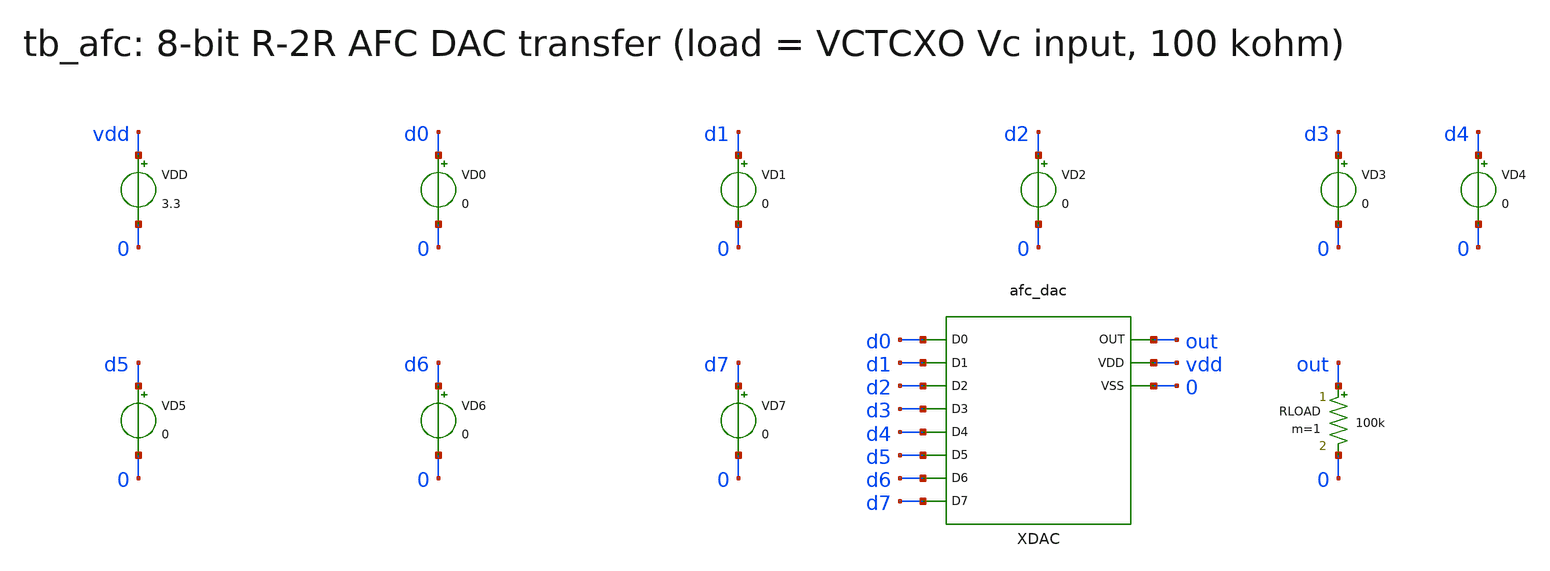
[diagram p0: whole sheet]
** sch_path: v1_claude/xschem/tb_afc.sch
**.subckt tb_afc
VDD vdd 0 3.3
VD0 d0 0 0
VD1 d1 0 0
VD2 d2 0 0
VD3 d3 0 0
VD4 d4 0 0
VD5 d5 0 0
VD6 d6 0 0
VD7 d7 0 0
XDAC d0 d1 d2 d3 d4 d5 d6 d7 out vdd 0 afc_dac
RLOAD out 0 100k m=1
**** begin user architecture code
 .include $::180MCU_MODELS/design.ngspice
.lib $::180MCU_MODELS/sm141064.ngspice typical
.lib $::180MCU_MODELS/sm141064.ngspice res_typical
.lib $::180MCU_MODELS/sm141064.ngspice mimcap_typical

.control
set num_threads=1
alter VD0 dc = 0
alter VD1 dc = 0
alter VD2 dc = 0
alter VD3 dc = 0
alter VD4 dc = 0
alter VD5 dc = 0
alter VD6 dc = 0
alter VD7 dc = 0
op
echo DAC 0 $&v(out)
alter VD0 dc = 3.3
alter VD1 dc = 0
alter VD2 dc = 0
alter VD3 dc = 0
alter VD4 dc = 0
alter VD5 dc = 0
alter VD6 dc = 0
alter VD7 dc = 0
op
echo DAC 1 $&v(out)
alter VD0 dc = 0
alter VD1 dc = 3.3
alter VD2 dc = 0
alter VD3 dc = 0
alter VD4 dc = 0
alter VD5 dc = 0
alter VD6 dc = 0
alter VD7 dc = 0
op
echo DAC 2 $&v(out)
alter VD0 dc = 3.3
alter VD1 dc = 3.3
alter VD2 dc = 0
alter VD3 dc = 0
alter VD4 dc = 0
alter VD5 dc = 0
alter VD6 dc = 0
alter VD7 dc = 0
op
echo DAC 3 $&v(out)
alter VD0 dc = 0
alter VD1 dc = 0
alter VD2 dc = 3.3
alter VD3 dc = 0
alter VD4 dc = 0
alter VD5 dc = 0
alter VD6 dc = 0
alter VD7 dc = 0
op
echo DAC 4 $&v(out)
alter VD0 dc = 3.3
alter VD1 dc = 0
alter VD2 dc = 3.3
alter VD3 dc = 0
alter VD4 dc = 0
alter VD5 dc = 0
alter VD6 dc = 0
alter VD7 dc = 0
op
echo DAC 5 $&v(out)
alter VD0 dc = 0
alter VD1 dc = 3.3
alter VD2 dc = 3.3
alter VD3 dc = 0
alter VD4 dc = 0
alter VD5 dc = 0
alter VD6 dc = 0
alter VD7 dc = 0
op
echo DAC 6 $&v(out)
alter VD0 dc = 3.3
alter VD1 dc = 3.3
alter VD2 dc = 3.3
alter VD3 dc = 0
alter VD4 dc = 0
alter VD5 dc = 0
alter VD6 dc = 0
alter VD7 dc = 0
op
echo DAC 7 $&v(out)
alter VD0 dc = 0
alter VD1 dc = 0
alter VD2 dc = 0
alter VD3 dc = 3.3
alter VD4 dc = 0
alter VD5 dc = 0
alter VD6 dc = 0
alter VD7 dc = 0
op
echo DAC 8 $&v(out)
alter VD0 dc = 3.3
alter VD1 dc = 0
alter VD2 dc = 0
alter VD3 dc = 3.3
alter VD4 dc = 0
alter VD5 dc = 0
alter VD6 dc = 0
alter VD7 dc = 0
op
echo DAC 9 $&v(out)
alter VD0 dc = 0
alter VD1 dc = 3.3
alter VD2 dc = 0
alter VD3 dc = 3.3
alter VD4 dc = 0
alter VD5 dc = 0
alter VD6 dc = 0
alter VD7 dc = 0
op
echo DAC 10 $&v(out)
alter VD0 dc = 3.3
alter VD1 dc = 3.3
alter VD2 dc = 0
alter VD3 dc = 3.3
alter VD4 dc = 0
alter VD5 dc = 0
alter VD6 dc = 0
alter VD7 dc = 0
op
echo DAC 11 $&v(out)
alter VD0 dc = 0
alter VD1 dc = 0
alter VD2 dc = 3.3
alter VD3 dc = 3.3
alter VD4 dc = 0
alter VD5 dc = 0
alter VD6 dc = 0
alter VD7 dc = 0
op
echo DAC 12 $&v(out)
alter VD0 dc = 3.3
alter VD1 dc = 0
alter VD2 dc = 3.3
alter VD3 dc = 3.3
alter VD4 dc = 0
alter VD5 dc = 0
alter VD6 dc = 0
alter VD7 dc = 0
op
echo DAC 13 $&v(out)
alter VD0 dc = 0
alter VD1 dc = 3.3
alter VD2 dc = 3.3
alter VD3 dc = 3.3
alter VD4 dc = 0
alter VD5 dc = 0
alter VD6 dc = 0
alter VD7 dc = 0
op
echo DAC 14 $&v(out)
alter VD0 dc = 3.3
alter VD1 dc = 3.3
alter VD2 dc = 3.3
alter VD3 dc = 3.3
alter VD4 dc = 0
alter VD5 dc = 0
alter VD6 dc = 0
alter VD7 dc = 0
op
echo DAC 15 $&v(out)
alter VD0 dc = 0
alter VD1 dc = 0
alter VD2 dc = 0
alter VD3 dc = 0
alter VD4 dc = 3.3
alter VD5 dc = 0
alter VD6 dc = 0
alter VD7 dc = 0
op
echo DAC 16 $&v(out)
alter VD0 dc = 3.3
alter VD1 dc = 0
alter VD2 dc = 0
alter VD3 dc = 0
alter VD4 dc = 3.3
alter VD5 dc = 0
alter VD6 dc = 0
alter VD7 dc = 0
op
echo DAC 17 $&v(out)
alter VD0 dc = 0
alter VD1 dc = 3.3
alter VD2 dc = 0
alter VD3 dc = 0
alter VD4 dc = 3.3
alter VD5 dc = 0
alter VD6 dc = 0
alter VD7 dc = 0
op
echo DAC 18 $&v(out)
alter VD0 dc = 3.3
alter VD1 dc = 3.3
alter VD2 dc = 0
alter VD3 dc = 0
alter VD4 dc = 3.3
alter VD5 dc = 0
alter VD6 dc = 0
alter VD7 dc = 0
op
echo DAC 19 $&v(out)
alter VD0 dc = 0
alter VD1 dc = 0
alter VD2 dc = 3.3
alter VD3 dc = 0
alter VD4 dc = 3.3
alter VD5 dc = 0
alter VD6 dc = 0
alter VD7 dc = 0
op
echo DAC 20 $&v(out)
alter VD0 dc = 3.3
alter VD1 dc = 0
alter VD2 dc = 3.3
alter VD3 dc = 0
alter VD4 dc = 3.3
alter VD5 dc = 0
alter VD6 dc = 0
alter VD7 dc = 0
op
echo DAC 21 $&v(out)
alter VD0 dc = 0
alter VD1 dc = 3.3
alter VD2 dc = 3.3
alter VD3 dc = 0
alter VD4 dc = 3.3
alter VD5 dc = 0
alter VD6 dc = 0
alter VD7 dc = 0
op
echo DAC 22 $&v(out)
alter VD0 dc = 3.3
alter VD1 dc = 3.3
alter VD2 dc = 3.3
alter VD3 dc = 0
alter VD4 dc = 3.3
alter VD5 dc = 0
alter VD6 dc = 0
alter VD7 dc = 0
op
echo DAC 23 $&v(out)
alter VD0 dc = 0
alter VD1 dc = 0
alter VD2 dc = 0
alter VD3 dc = 3.3
alter VD4 dc = 3.3
alter VD5 dc = 0
alter VD6 dc = 0
alter VD7 dc = 0
op
echo DAC 24 $&v(out)
alter VD0 dc = 3.3
alter VD1 dc = 0
alter VD2 dc = 0
alter VD3 dc = 3.3
alter VD4 dc = 3.3
alter VD5 dc = 0
alter VD6 dc = 0
alter VD7 dc = 0
op
echo DAC 25 $&v(out)
alter VD0 dc = 0
alter VD1 dc = 3.3
alter VD2 dc = 0
alter VD3 dc = 3.3
alter VD4 dc = 3.3
alter VD5 dc = 0
alter VD6 dc = 0
alter VD7 dc = 0
op
echo DAC 26 $&v(out)
alter VD0 dc = 3.3
alter VD1 dc = 3.3
alter VD2 dc = 0
alter VD3 dc = 3.3
alter VD4 dc = 3.3
alter VD5 dc = 0
alter VD6 dc = 0
alter VD7 dc = 0
op
echo DAC 27 $&v(out)
alter VD0 dc = 0
alter VD1 dc = 0
alter VD2 dc = 3.3
alter VD3 dc = 3.3
alter VD4 dc = 3.3
alter VD5 dc = 0
alter VD6 dc = 0
alter VD7 dc = 0
op
echo DAC 28 $&v(out)
alter VD0 dc = 3.3
alter VD1 dc = 0
alter VD2 dc = 3.3
alter VD3 dc = 3.3
alter VD4 dc = 3.3
alter VD5 dc = 0
alter VD6 dc = 0
alter VD7 dc = 0
op
echo DAC 29 $&v(out)
alter VD0 dc = 0
alter VD1 dc = 3.3
alter VD2 dc = 3.3
alter VD3 dc = 3.3
alter VD4 dc = 3.3
alter VD5 dc = 0
alter VD6 dc = 0
alter VD7 dc = 0
op
echo DAC 30 $&v(out)
alter VD0 dc = 3.3
alter VD1 dc = 3.3
alter VD2 dc = 3.3
alter VD3 dc = 3.3
alter VD4 dc = 3.3
alter VD5 dc = 0
alter VD6 dc = 0
alter VD7 dc = 0
op
echo DAC 31 $&v(out)
alter VD0 dc = 0
alter VD1 dc = 0
alter VD2 dc = 0
alter VD3 dc = 0
alter VD4 dc = 0
alter VD5 dc = 3.3
alter VD6 dc = 0
alter VD7 dc = 0
op
echo DAC 32 $&v(out)
alter VD0 dc = 3.3
alter VD1 dc = 0
alter VD2 dc = 0
alter VD3 dc = 0
alter VD4 dc = 0
alter VD5 dc = 3.3
alter VD6 dc = 0
alter VD7 dc = 0
op
echo DAC 33 $&v(out)
alter VD0 dc = 0
alter VD1 dc = 3.3
alter VD2 dc = 0
alter VD3 dc = 0
alter VD4 dc = 0
alter VD5 dc = 3.3
alter VD6 dc = 0
alter VD7 dc = 0
op
echo DAC 34 $&v(out)
alter VD0 dc = 3.3
alter VD1 dc = 3.3
alter VD2 dc = 0
alter VD3 dc = 0
alter VD4 dc = 0
alter VD5 dc = 3.3
alter VD6 dc = 0
alter VD7 dc = 0
op
echo DAC 35 $&v(out)
alter VD0 dc = 0
alter VD1 dc = 0
alter VD2 dc = 3.3
alter VD3 dc = 0
alter VD4 dc = 0
alter VD5 dc = 3.3
alter VD6 dc = 0
alter VD7 dc = 0
op
echo DAC 36 $&v(out)
alter VD0 dc = 3.3
alter VD1 dc = 0
alter VD2 dc = 3.3
alter VD3 dc = 0
alter VD4 dc = 0
alter VD5 dc = 3.3
alter VD6 dc = 0
alter VD7 dc = 0
op
echo DAC 37 $&v(out)
alter VD0 dc = 0
alter VD1 dc = 3.3
alter VD2 dc = 3.3
alter VD3 dc = 0
alter VD4 dc = 0
alter VD5 dc = 3.3
alter VD6 dc = 0
alter VD7 dc = 0
op
echo DAC 38 $&v(out)
alter VD0 dc = 3.3
alter VD1 dc = 3.3
alter VD2 dc = 3.3
alter VD3 dc = 0
alter VD4 dc = 0
alter VD5 dc = 3.3
alter VD6 dc = 0
alter VD7 dc = 0
op
echo DAC 39 $&v(out)
alter VD0 dc = 0
alter VD1 dc = 0
alter VD2 dc = 0
alter VD3 dc = 3.3
alter VD4 dc = 0
alter VD5 dc = 3.3
alter VD6 dc = 0
alter VD7 dc = 0
op
echo DAC 40 $&v(out)
alter VD0 dc = 3.3
alter VD1 dc = 0
alter VD2 dc = 0
alter VD3 dc = 3.3
alter VD4 dc = 0
alter VD5 dc = 3.3
alter VD6 dc = 0
alter VD7 dc = 0
op
echo DAC 41 $&v(out)
alter VD0 dc = 0
alter VD1 dc = 3.3
alter VD2 dc = 0
alter VD3 dc = 3.3
alter VD4 dc = 0
alter VD5 dc = 3.3
alter VD6 dc = 0
alter VD7 dc = 0
op
echo DAC 42 $&v(out)
alter VD0 dc = 3.3
alter VD1 dc = 3.3
alter VD2 dc = 0
alter VD3 dc = 3.3
alter VD4 dc = 0
alter VD5 dc = 3.3
alter VD6 dc = 0
alter VD7 dc = 0
op
echo DAC 43 $&v(out)
alter VD0 dc = 0
alter VD1 dc = 0
alter VD2 dc = 3.3
alter VD3 dc = 3.3
alter VD4 dc = 0
alter VD5 dc = 3.3
alter VD6 dc = 0
alter VD7 dc = 0
op
echo DAC 44 $&v(out)
alter VD0 dc = 3.3
alter VD1 dc = 0
alter VD2 dc = 3.3
alter VD3 dc = 3.3
alter VD4 dc = 0
alter VD5 dc = 3.3
alter VD6 dc = 0
alter VD7 dc = 0
op
echo DAC 45 $&v(out)
alter VD0 dc = 0
alter VD1 dc = 3.3
alter VD2 dc = 3.3
alter VD3 dc = 3.3
alter VD4 dc = 0
alter VD5 dc = 3.3
alter VD6 dc = 0
alter VD7 dc = 0
op
echo DAC 46 $&v(out)
alter VD0 dc = 3.3
alter VD1 dc = 3.3
alter VD2 dc = 3.3
alter VD3 dc = 3.3
alter VD4 dc = 0
alter VD5 dc = 3.3
alter VD6 dc = 0
alter VD7 dc = 0
op
echo DAC 47 $&v(out)
alter VD0 dc = 0
alter VD1 dc = 0
alter VD2 dc = 0
alter VD3 dc = 0
alter VD4 dc = 3.3
alter VD5 dc = 3.3
alter VD6 dc = 0
alter VD7 dc = 0
op
echo DAC 48 $&v(out)
alter VD0 dc = 3.3
alter VD1 dc = 0
alter VD2 dc = 0
alter VD3 dc = 0
alter VD4 dc = 3.3
alter VD5 dc = 3.3
alter VD6 dc = 0
alter VD7 dc = 0
op
echo DAC 49 $&v(out)
alter VD0 dc = 0
alter VD1 dc = 3.3
alter VD2 dc = 0
alter VD3 dc = 0
alter VD4 dc = 3.3
alter VD5 dc = 3.3
alter VD6 dc = 0
alter VD7 dc = 0
op
echo DAC 50 $&v(out)
alter VD0 dc = 3.3
alter VD1 dc = 3.3
alter VD2 dc = 0
alter VD3 dc = 0
alter VD4 dc = 3.3
alter VD5 dc = 3.3
alter VD6 dc = 0
alter VD7 dc = 0
op
echo DAC 51 $&v(out)
alter VD0 dc = 0
alter VD1 dc = 0
alter VD2 dc = 3.3
alter VD3 dc = 0
alter VD4 dc = 3.3
alter VD5 dc = 3.3
alter VD6 dc = 0
alter VD7 dc = 0
op
echo DAC 52 $&v(out)
alter VD0 dc = 3.3
alter VD1 dc = 0
alter VD2 dc = 3.3
alter VD3 dc = 0
alter VD4 dc = 3.3
alter VD5 dc = 3.3
alter VD6 dc = 0
alter VD7 dc = 0
op
echo DAC 53 $&v(out)
alter VD0 dc = 0
alter VD1 dc = 3.3
alter VD2 dc = 3.3
alter VD3 dc = 0
alter VD4 dc = 3.3
alter VD5 dc = 3.3
alter VD6 dc = 0
alter VD7 dc = 0
op
echo DAC 54 $&v(out)
alter VD0 dc = 3.3
alter VD1 dc = 3.3
alter VD2 dc = 3.3
alter VD3 dc = 0
alter VD4 dc = 3.3
alter VD5 dc = 3.3
alter VD6 dc = 0
alter VD7 dc = 0
op
echo DAC 55 $&v(out)
alter VD0 dc = 0
alter VD1 dc = 0
alter VD2 dc = 0
alter VD3 dc = 3.3
alter VD4 dc = 3.3
alter VD5 dc = 3.3
alter VD6 dc = 0
alter VD7 dc = 0
op
echo DAC 56 $&v(out)
alter VD0 dc = 3.3
alter VD1 dc = 0
alter VD2 dc = 0
alter VD3 dc = 3.3
alter VD4 dc = 3.3
alter VD5 dc = 3.3
alter VD6 dc = 0
alter VD7 dc = 0
op
echo DAC 57 $&v(out)
alter VD0 dc = 0
alter VD1 dc = 3.3
alter VD2 dc = 0
alter VD3 dc = 3.3
alter VD4 dc = 3.3
alter VD5 dc = 3.3
alter VD6 dc = 0
alter VD7 dc = 0
op
echo DAC 58 $&v(out)
alter VD0 dc = 3.3
alter VD1 dc = 3.3
alter VD2 dc = 0
alter VD3 dc = 3.3
alter VD4 dc = 3.3
alter VD5 dc = 3.3
alter VD6 dc = 0
alter VD7 dc = 0
op
echo DAC 59 $&v(out)
alter VD0 dc = 0
alter VD1 dc = 0
alter VD2 dc = 3.3
alter VD3 dc = 3.3
alter VD4 dc = 3.3
alter VD5 dc = 3.3
alter VD6 dc = 0
alter VD7 dc = 0
op
echo DAC 60 $&v(out)
alter VD0 dc = 3.3
alter VD1 dc = 0
alter VD2 dc = 3.3
alter VD3 dc = 3.3
alter VD4 dc = 3.3
alter VD5 dc = 3.3
alter VD6 dc = 0
alter VD7 dc = 0
op
echo DAC 61 $&v(out)
alter VD0 dc = 0
alter VD1 dc = 3.3
alter VD2 dc = 3.3
alter VD3 dc = 3.3
alter VD4 dc = 3.3
alter VD5 dc = 3.3
alter VD6 dc = 0
alter VD7 dc = 0
op
echo DAC 62 $&v(out)
alter VD0 dc = 3.3
alter VD1 dc = 3.3
alter VD2 dc = 3.3
alter VD3 dc = 3.3
alter VD4 dc = 3.3
alter VD5 dc = 3.3
alter VD6 dc = 0
alter VD7 dc = 0
op
echo DAC 63 $&v(out)
alter VD0 dc = 0
alter VD1 dc = 0
alter VD2 dc = 0
alter VD3 dc = 0
alter VD4 dc = 0
alter VD5 dc = 0
alter VD6 dc = 3.3
alter VD7 dc = 0
op
echo DAC 64 $&v(out)
alter VD0 dc = 3.3
alter VD1 dc = 0
alter VD2 dc = 0
alter VD3 dc = 0
alter VD4 dc = 0
alter VD5 dc = 0
alter VD6 dc = 3.3
alter VD7 dc = 0
op
echo DAC 65 $&v(out)
alter VD0 dc = 0
alter VD1 dc = 3.3
alter VD2 dc = 0
alter VD3 dc = 0
alter VD4 dc = 0
alter VD5 dc = 0
alter VD6 dc = 3.3
alter VD7 dc = 0
op
echo DAC 66 $&v(out)
alter VD0 dc = 3.3
alter VD1 dc = 3.3
alter VD2 dc = 0
alter VD3 dc = 0
alter VD4 dc = 0
alter VD5 dc = 0
alter VD6 dc = 3.3
alter VD7 dc = 0
op
echo DAC 67 $&v(out)
alter VD0 dc = 0
alter VD1 dc = 0
alter VD2 dc = 3.3
alter VD3 dc = 0
alter VD4 dc = 0
alter VD5 dc = 0
alter VD6 dc = 3.3
alter VD7 dc = 0
op
echo DAC 68 $&v(out)
alter VD0 dc = 3.3
alter VD1 dc = 0
alter VD2 dc = 3.3
alter VD3 dc = 0
alter VD4 dc = 0
alter VD5 dc = 0
alter VD6 dc = 3.3
alter VD7 dc = 0
op
echo DAC 69 $&v(out)
alter VD0 dc = 0
alter VD1 dc = 3.3
alter VD2 dc = 3.3
alter VD3 dc = 0
alter VD4 dc = 0
alter VD5 dc = 0
alter VD6 dc = 3.3
alter VD7 dc = 0
op
echo DAC 70 $&v(out)
alter VD0 dc = 3.3
alter VD1 dc = 3.3
alter VD2 dc = 3.3
alter VD3 dc = 0
alter VD4 dc = 0
alter VD5 dc = 0
alter VD6 dc = 3.3
alter VD7 dc = 0
op
echo DAC 71 $&v(out)
alter VD0 dc = 0
alter VD1 dc = 0
alter VD2 dc = 0
alter VD3 dc = 3.3
alter VD4 dc = 0
alter VD5 dc = 0
alter VD6 dc = 3.3
alter VD7 dc = 0
op
echo DAC 72 $&v(out)
alter VD0 dc = 3.3
alter VD1 dc = 0
alter VD2 dc = 0
alter VD3 dc = 3.3
alter VD4 dc = 0
alter VD5 dc = 0
alter VD6 dc = 3.3
alter VD7 dc = 0
op
echo DAC 73 $&v(out)
alter VD0 dc = 0
alter VD1 dc = 3.3
alter VD2 dc = 0
alter VD3 dc = 3.3
alter VD4 dc = 0
alter VD5 dc = 0
alter VD6 dc = 3.3
alter VD7 dc = 0
op
echo DAC 74 $&v(out)
alter VD0 dc = 3.3
alter VD1 dc = 3.3
alter VD2 dc = 0
alter VD3 dc = 3.3
alter VD4 dc = 0
alter VD5 dc = 0
alter VD6 dc = 3.3
alter VD7 dc = 0
op
echo DAC 75 $&v(out)
alter VD0 dc = 0
alter VD1 dc = 0
alter VD2 dc = 3.3
alter VD3 dc = 3.3
alter VD4 dc = 0
alter VD5 dc = 0
alter VD6 dc = 3.3
alter VD7 dc = 0
op
echo DAC 76 $&v(out)
alter VD0 dc = 3.3
alter VD1 dc = 0
alter VD2 dc = 3.3
alter VD3 dc = 3.3
alter VD4 dc = 0
alter VD5 dc = 0
alter VD6 dc = 3.3
alter VD7 dc = 0
op
echo DAC 77 $&v(out)
alter VD0 dc = 0
alter VD1 dc = 3.3
alter VD2 dc = 3.3
alter VD3 dc = 3.3
alter VD4 dc = 0
alter VD5 dc = 0
alter VD6 dc = 3.3
alter VD7 dc = 0
op
echo DAC 78 $&v(out)
alter VD0 dc = 3.3
alter VD1 dc = 3.3
alter VD2 dc = 3.3
alter VD3 dc = 3.3
alter VD4 dc = 0
alter VD5 dc = 0
alter VD6 dc = 3.3
alter VD7 dc = 0
op
echo DAC 79 $&v(out)
alter VD0 dc = 0
alter VD1 dc = 0
alter VD2 dc = 0
alter VD3 dc = 0
alter VD4 dc = 3.3
alter VD5 dc = 0
alter VD6 dc = 3.3
alter VD7 dc = 0
op
echo DAC 80 $&v(out)
alter VD0 dc = 3.3
alter VD1 dc = 0
alter VD2 dc = 0
alter VD3 dc = 0
alter VD4 dc = 3.3
alter VD5 dc = 0
alter VD6 dc = 3.3
alter VD7 dc = 0
op
echo DAC 81 $&v(out)
alter VD0 dc = 0
alter VD1 dc = 3.3
alter VD2 dc = 0
alter VD3 dc = 0
alter VD4 dc = 3.3
alter VD5 dc = 0
alter VD6 dc = 3.3
alter VD7 dc = 0
op
echo DAC 82 $&v(out)
alter VD0 dc = 3.3
alter VD1 dc = 3.3
alter VD2 dc = 0
alter VD3 dc = 0
alter VD4 dc = 3.3
alter VD5 dc = 0
alter VD6 dc = 3.3
alter VD7 dc = 0
op
echo DAC 83 $&v(out)
alter VD0 dc = 0
alter VD1 dc = 0
alter VD2 dc = 3.3
alter VD3 dc = 0
alter VD4 dc = 3.3
alter VD5 dc = 0
alter VD6 dc = 3.3
alter VD7 dc = 0
op
echo DAC 84 $&v(out)
alter VD0 dc = 3.3
alter VD1 dc = 0
alter VD2 dc = 3.3
alter VD3 dc = 0
alter VD4 dc = 3.3
alter VD5 dc = 0
alter VD6 dc = 3.3
alter VD7 dc = 0
op
echo DAC 85 $&v(out)
alter VD0 dc = 0
alter VD1 dc = 3.3
alter VD2 dc = 3.3
alter VD3 dc = 0
alter VD4 dc = 3.3
alter VD5 dc = 0
alter VD6 dc = 3.3
alter VD7 dc = 0
op
echo DAC 86 $&v(out)
alter VD0 dc = 3.3
alter VD1 dc = 3.3
alter VD2 dc = 3.3
alter VD3 dc = 0
alter VD4 dc = 3.3
alter VD5 dc = 0
alter VD6 dc = 3.3
alter VD7 dc = 0
op
echo DAC 87 $&v(out)
alter VD0 dc = 0
alter VD1 dc = 0
alter VD2 dc = 0
alter VD3 dc = 3.3
alter VD4 dc = 3.3
alter VD5 dc = 0
alter VD6 dc = 3.3
alter VD7 dc = 0
op
echo DAC 88 $&v(out)
alter VD0 dc = 3.3
alter VD1 dc = 0
alter VD2 dc = 0
alter VD3 dc = 3.3
alter VD4 dc = 3.3
alter VD5 dc = 0
alter VD6 dc = 3.3
alter VD7 dc = 0
op
echo DAC 89 $&v(out)
alter VD0 dc = 0
alter VD1 dc = 3.3
alter VD2 dc = 0
alter VD3 dc = 3.3
alter VD4 dc = 3.3
alter VD5 dc = 0
alter VD6 dc = 3.3
alter VD7 dc = 0
op
echo DAC 90 $&v(out)
alter VD0 dc = 3.3
alter VD1 dc = 3.3
alter VD2 dc = 0
alter VD3 dc = 3.3
alter VD4 dc = 3.3
alter VD5 dc = 0
alter VD6 dc = 3.3
alter VD7 dc = 0
op
echo DAC 91 $&v(out)
alter VD0 dc = 0
alter VD1 dc = 0
alter VD2 dc = 3.3
alter VD3 dc = 3.3
alter VD4 dc = 3.3
alter VD5 dc = 0
alter VD6 dc = 3.3
alter VD7 dc = 0
op
echo DAC 92 $&v(out)
alter VD0 dc = 3.3
alter VD1 dc = 0
alter VD2 dc = 3.3
alter VD3 dc = 3.3
alter VD4 dc = 3.3
alter VD5 dc = 0
alter VD6 dc = 3.3
alter VD7 dc = 0
op
echo DAC 93 $&v(out)
alter VD0 dc = 0
alter VD1 dc = 3.3
alter VD2 dc = 3.3
alter VD3 dc = 3.3
alter VD4 dc = 3.3
alter VD5 dc = 0
alter VD6 dc = 3.3
alter VD7 dc = 0
op
echo DAC 94 $&v(out)
alter VD0 dc = 3.3
alter VD1 dc = 3.3
alter VD2 dc = 3.3
alter VD3 dc = 3.3
alter VD4 dc = 3.3
alter VD5 dc = 0
alter VD6 dc = 3.3
alter VD7 dc = 0
op
echo DAC 95 $&v(out)
alter VD0 dc = 0
alter VD1 dc = 0
alter VD2 dc = 0
alter VD3 dc = 0
alter VD4 dc = 0
alter VD5 dc = 3.3
alter VD6 dc = 3.3
alter VD7 dc = 0
op
echo DAC 96 $&v(out)
alter VD0 dc = 3.3
alter VD1 dc = 0
alter VD2 dc = 0
alter VD3 dc = 0
alter VD4 dc = 0
alter VD5 dc = 3.3
alter VD6 dc = 3.3
alter VD7 dc = 0
op
echo DAC 97 $&v(out)
alter VD0 dc = 0
alter VD1 dc = 3.3
alter VD2 dc = 0
alter VD3 dc = 0
alter VD4 dc = 0
alter VD5 dc = 3.3
alter VD6 dc = 3.3
alter VD7 dc = 0
op
echo DAC 98 $&v(out)
alter VD0 dc = 3.3
alter VD1 dc = 3.3
alter VD2 dc = 0
alter VD3 dc = 0
alter VD4 dc = 0
alter VD5 dc = 3.3
alter VD6 dc = 3.3
alter VD7 dc = 0
op
echo DAC 99 $&v(out)
alter VD0 dc = 0
alter VD1 dc = 0
alter VD2 dc = 3.3
alter VD3 dc = 0
alter VD4 dc = 0
alter VD5 dc = 3.3
alter VD6 dc = 3.3
alter VD7 dc = 0
op
echo DAC 100 $&v(out)
alter VD0 dc = 3.3
alter VD1 dc = 0
alter VD2 dc = 3.3
alter VD3 dc = 0
alter VD4 dc = 0
alter VD5 dc = 3.3
alter VD6 dc = 3.3
alter VD7 dc = 0
op
echo DAC 101 $&v(out)
alter VD0 dc = 0
alter VD1 dc = 3.3
alter VD2 dc = 3.3
alter VD3 dc = 0
alter VD4 dc = 0
alter VD5 dc = 3.3
alter VD6 dc = 3.3
alter VD7 dc = 0
op
echo DAC 102 $&v(out)
alter VD0 dc = 3.3
alter VD1 dc = 3.3
alter VD2 dc = 3.3
alter VD3 dc = 0
alter VD4 dc = 0
alter VD5 dc = 3.3
alter VD6 dc = 3.3
alter VD7 dc = 0
op
echo DAC 103 $&v(out)
alter VD0 dc = 0
alter VD1 dc = 0
alter VD2 dc = 0
alter VD3 dc = 3.3
alter VD4 dc = 0
alter VD5 dc = 3.3
alter VD6 dc = 3.3
alter VD7 dc = 0
op
echo DAC 104 $&v(out)
alter VD0 dc = 3.3
alter VD1 dc = 0
alter VD2 dc = 0
alter VD3 dc = 3.3
alter VD4 dc = 0
alter VD5 dc = 3.3
alter VD6 dc = 3.3
alter VD7 dc = 0
op
echo DAC 105 $&v(out)
alter VD0 dc = 0
alter VD1 dc = 3.3
alter VD2 dc = 0
alter VD3 dc = 3.3
alter VD4 dc = 0
alter VD5 dc = 3.3
alter VD6 dc = 3.3
alter VD7 dc = 0
op
echo DAC 106 $&v(out)
alter VD0 dc = 3.3
alter VD1 dc = 3.3
alter VD2 dc = 0
alter VD3 dc = 3.3
alter VD4 dc = 0
alter VD5 dc = 3.3
alter VD6 dc = 3.3
alter VD7 dc = 0
op
echo DAC 107 $&v(out)
alter VD0 dc = 0
alter VD1 dc = 0
alter VD2 dc = 3.3
alter VD3 dc = 3.3
alter VD4 dc = 0
alter VD5 dc = 3.3
alter VD6 dc = 3.3
alter VD7 dc = 0
op
echo DAC 108 $&v(out)
alter VD0 dc = 3.3
alter VD1 dc = 0
alter VD2 dc = 3.3
alter VD3 dc = 3.3
alter VD4 dc = 0
alter VD5 dc = 3.3
alter VD6 dc = 3.3
alter VD7 dc = 0
op
echo DAC 109 $&v(out)
alter VD0 dc = 0
alter VD1 dc = 3.3
alter VD2 dc = 3.3
alter VD3 dc = 3.3
alter VD4 dc = 0
alter VD5 dc = 3.3
alter VD6 dc = 3.3
alter VD7 dc = 0
op
echo DAC 110 $&v(out)
alter VD0 dc = 3.3
alter VD1 dc = 3.3
alter VD2 dc = 3.3
alter VD3 dc = 3.3
alter VD4 dc = 0
alter VD5 dc = 3.3
alter VD6 dc = 3.3
alter VD7 dc = 0
op
echo DAC 111 $&v(out)
alter VD0 dc = 0
alter VD1 dc = 0
alter VD2 dc = 0
alter VD3 dc = 0
alter VD4 dc = 3.3
alter VD5 dc = 3.3
alter VD6 dc = 3.3
alter VD7 dc = 0
op
echo DAC 112 $&v(out)
alter VD0 dc = 3.3
alter VD1 dc = 0
alter VD2 dc = 0
alter VD3 dc = 0
alter VD4 dc = 3.3
alter VD5 dc = 3.3
alter VD6 dc = 3.3
alter VD7 dc = 0
op
echo DAC 113 $&v(out)
alter VD0 dc = 0
alter VD1 dc = 3.3
alter VD2 dc = 0
alter VD3 dc = 0
alter VD4 dc = 3.3
alter VD5 dc = 3.3
alter VD6 dc = 3.3
alter VD7 dc = 0
op
echo DAC 114 $&v(out)
alter VD0 dc = 3.3
alter VD1 dc = 3.3
alter VD2 dc = 0
alter VD3 dc = 0
alter VD4 dc = 3.3
alter VD5 dc = 3.3
alter VD6 dc = 3.3
alter VD7 dc = 0
op
echo DAC 115 $&v(out)
alter VD0 dc = 0
alter VD1 dc = 0
alter VD2 dc = 3.3
alter VD3 dc = 0
alter VD4 dc = 3.3
alter VD5 dc = 3.3
alter VD6 dc = 3.3
alter VD7 dc = 0
op
echo DAC 116 $&v(out)
alter VD0 dc = 3.3
alter VD1 dc = 0
alter VD2 dc = 3.3
alter VD3 dc = 0
alter VD4 dc = 3.3
alter VD5 dc = 3.3
alter VD6 dc = 3.3
alter VD7 dc = 0
op
echo DAC 117 $&v(out)
alter VD0 dc = 0
alter VD1 dc = 3.3
alter VD2 dc = 3.3
alter VD3 dc = 0
alter VD4 dc = 3.3
alter VD5 dc = 3.3
alter VD6 dc = 3.3
alter VD7 dc = 0
op
echo DAC 118 $&v(out)
alter VD0 dc = 3.3
alter VD1 dc = 3.3
alter VD2 dc = 3.3
alter VD3 dc = 0
alter VD4 dc = 3.3
alter VD5 dc = 3.3
alter VD6 dc = 3.3
alter VD7 dc = 0
op
echo DAC 119 $&v(out)
alter VD0 dc = 0
alter VD1 dc = 0
alter VD2 dc = 0
alter VD3 dc = 3.3
alter VD4 dc = 3.3
alter VD5 dc = 3.3
alter VD6 dc = 3.3
alter VD7 dc = 0
op
echo DAC 120 $&v(out)
alter VD0 dc = 3.3
alter VD1 dc = 0
alter VD2 dc = 0
alter VD3 dc = 3.3
alter VD4 dc = 3.3
alter VD5 dc = 3.3
alter VD6 dc = 3.3
alter VD7 dc = 0
op
echo DAC 121 $&v(out)
alter VD0 dc = 0
alter VD1 dc = 3.3
alter VD2 dc = 0
alter VD3 dc = 3.3
alter VD4 dc = 3.3
alter VD5 dc = 3.3
alter VD6 dc = 3.3
alter VD7 dc = 0
op
echo DAC 122 $&v(out)
alter VD0 dc = 3.3
alter VD1 dc = 3.3
alter VD2 dc = 0
alter VD3 dc = 3.3
alter VD4 dc = 3.3
alter VD5 dc = 3.3
alter VD6 dc = 3.3
alter VD7 dc = 0
op
echo DAC 123 $&v(out)
alter VD0 dc = 0
alter VD1 dc = 0
alter VD2 dc = 3.3
alter VD3 dc = 3.3
alter VD4 dc = 3.3
alter VD5 dc = 3.3
alter VD6 dc = 3.3
alter VD7 dc = 0
op
echo DAC 124 $&v(out)
alter VD0 dc = 3.3
alter VD1 dc = 0
alter VD2 dc = 3.3
alter VD3 dc = 3.3
alter VD4 dc = 3.3
alter VD5 dc = 3.3
alter VD6 dc = 3.3
alter VD7 dc = 0
op
echo DAC 125 $&v(out)
alter VD0 dc = 0
alter VD1 dc = 3.3
alter VD2 dc = 3.3
alter VD3 dc = 3.3
alter VD4 dc = 3.3
alter VD5 dc = 3.3
alter VD6 dc = 3.3
alter VD7 dc = 0
op
echo DAC 126 $&v(out)
alter VD0 dc = 3.3
alter VD1 dc = 3.3
alter VD2 dc = 3.3
alter VD3 dc = 3.3
alter VD4 dc = 3.3
alter VD5 dc = 3.3
alter VD6 dc = 3.3
alter VD7 dc = 0
op
echo DAC 127 $&v(out)
alter VD0 dc = 0
alter VD1 dc = 0
alter VD2 dc = 0
alter VD3 dc = 0
alter VD4 dc = 0
alter VD5 dc = 0
alter VD6 dc = 0
alter VD7 dc = 3.3
op
echo DAC 128 $&v(out)
alter VD0 dc = 3.3
alter VD1 dc = 0
alter VD2 dc = 0
alter VD3 dc = 0
alter VD4 dc = 0
alter VD5 dc = 0
alter VD6 dc = 0
alter VD7 dc = 3.3
op
echo DAC 129 $&v(out)
alter VD0 dc = 0
alter VD1 dc = 3.3
alter VD2 dc = 0
alter VD3 dc = 0
alter VD4 dc = 0
alter VD5 dc = 0
alter VD6 dc = 0
alter VD7 dc = 3.3
op
echo DAC 130 $&v(out)
alter VD0 dc = 3.3
alter VD1 dc = 3.3
alter VD2 dc = 0
alter VD3 dc = 0
alter VD4 dc = 0
alter VD5 dc = 0
alter VD6 dc = 0
alter VD7 dc = 3.3
op
echo DAC 131 $&v(out)
alter VD0 dc = 0
alter VD1 dc = 0
alter VD2 dc = 3.3
alter VD3 dc = 0
alter VD4 dc = 0
alter VD5 dc = 0
alter VD6 dc = 0
alter VD7 dc = 3.3
op
echo DAC 132 $&v(out)
alter VD0 dc = 3.3
alter VD1 dc = 0
alter VD2 dc = 3.3
alter VD3 dc = 0
alter VD4 dc = 0
alter VD5 dc = 0
alter VD6 dc = 0
alter VD7 dc = 3.3
op
echo DAC 133 $&v(out)
alter VD0 dc = 0
alter VD1 dc = 3.3
alter VD2 dc = 3.3
alter VD3 dc = 0
alter VD4 dc = 0
alter VD5 dc = 0
alter VD6 dc = 0
alter VD7 dc = 3.3
op
echo DAC 134 $&v(out)
alter VD0 dc = 3.3
alter VD1 dc = 3.3
alter VD2 dc = 3.3
alter VD3 dc = 0
alter VD4 dc = 0
alter VD5 dc = 0
alter VD6 dc = 0
alter VD7 dc = 3.3
op
echo DAC 135 $&v(out)
alter VD0 dc = 0
alter VD1 dc = 0
alter VD2 dc = 0
alter VD3 dc = 3.3
alter VD4 dc = 0
alter VD5 dc = 0
alter VD6 dc = 0
alter VD7 dc = 3.3
op
echo DAC 136 $&v(out)
alter VD0 dc = 3.3
alter VD1 dc = 0
alter VD2 dc = 0
alter VD3 dc = 3.3
alter VD4 dc = 0
alter VD5 dc = 0
alter VD6 dc = 0
alter VD7 dc = 3.3
op
echo DAC 137 $&v(out)
alter VD0 dc = 0
alter VD1 dc = 3.3
alter VD2 dc = 0
alter VD3 dc = 3.3
alter VD4 dc = 0
alter VD5 dc = 0
alter VD6 dc = 0
alter VD7 dc = 3.3
op
echo DAC 138 $&v(out)
alter VD0 dc = 3.3
alter VD1 dc = 3.3
alter VD2 dc = 0
alter VD3 dc = 3.3
alter VD4 dc = 0
alter VD5 dc = 0
alter VD6 dc = 0
alter VD7 dc = 3.3
op
echo DAC 139 $&v(out)
alter VD0 dc = 0
alter VD1 dc = 0
alter VD2 dc = 3.3
alter VD3 dc = 3.3
alter VD4 dc = 0
alter VD5 dc = 0
alter VD6 dc = 0
alter VD7 dc = 3.3
op
echo DAC 140 $&v(out)
alter VD0 dc = 3.3
alter VD1 dc = 0
alter VD2 dc = 3.3
alter VD3 dc = 3.3
alter VD4 dc = 0
alter VD5 dc = 0
alter VD6 dc = 0
alter VD7 dc = 3.3
op
echo DAC 141 $&v(out)
alter VD0 dc = 0
alter VD1 dc = 3.3
alter VD2 dc = 3.3
alter VD3 dc = 3.3
alter VD4 dc = 0
alter VD5 dc = 0
alter VD6 dc = 0
alter VD7 dc = 3.3
op
echo DAC 142 $&v(out)
alter VD0 dc = 3.3
alter VD1 dc = 3.3
alter VD2 dc = 3.3
alter VD3 dc = 3.3
alter VD4 dc = 0
alter VD5 dc = 0
alter VD6 dc = 0
alter VD7 dc = 3.3
op
echo DAC 143 $&v(out)
alter VD0 dc = 0
alter VD1 dc = 0
alter VD2 dc = 0
alter VD3 dc = 0
alter VD4 dc = 3.3
alter VD5 dc = 0
alter VD6 dc = 0
alter VD7 dc = 3.3
op
echo DAC 144 $&v(out)
alter VD0 dc = 3.3
alter VD1 dc = 0
alter VD2 dc = 0
alter VD3 dc = 0
alter VD4 dc = 3.3
alter VD5 dc = 0
alter VD6 dc = 0
alter VD7 dc = 3.3
op
echo DAC 145 $&v(out)
alter VD0 dc = 0
alter VD1 dc = 3.3
alter VD2 dc = 0
alter VD3 dc = 0
alter VD4 dc = 3.3
alter VD5 dc = 0
alter VD6 dc = 0
alter VD7 dc = 3.3
op
echo DAC 146 $&v(out)
alter VD0 dc = 3.3
alter VD1 dc = 3.3
alter VD2 dc = 0
alter VD3 dc = 0
alter VD4 dc = 3.3
alter VD5 dc = 0
alter VD6 dc = 0
alter VD7 dc = 3.3
op
echo DAC 147 $&v(out)
alter VD0 dc = 0
alter VD1 dc = 0
alter VD2 dc = 3.3
alter VD3 dc = 0
alter VD4 dc = 3.3
alter VD5 dc = 0
alter VD6 dc = 0
alter VD7 dc = 3.3
op
echo DAC 148 $&v(out)
alter VD0 dc = 3.3
alter VD1 dc = 0
alter VD2 dc = 3.3
alter VD3 dc = 0
alter VD4 dc = 3.3
alter VD5 dc = 0
alter VD6 dc = 0
alter VD7 dc = 3.3
op
echo DAC 149 $&v(out)
alter VD0 dc = 0
alter VD1 dc = 3.3
alter VD2 dc = 3.3
alter VD3 dc = 0
alter VD4 dc = 3.3
alter VD5 dc = 0
alter VD6 dc = 0
alter VD7 dc = 3.3
op
echo DAC 150 $&v(out)
alter VD0 dc = 3.3
alter VD1 dc = 3.3
alter VD2 dc = 3.3
alter VD3 dc = 0
alter VD4 dc = 3.3
alter VD5 dc = 0
alter VD6 dc = 0
alter VD7 dc = 3.3
op
echo DAC 151 $&v(out)
alter VD0 dc = 0
alter VD1 dc = 0
alter VD2 dc = 0
alter VD3 dc = 3.3
alter VD4 dc = 3.3
alter VD5 dc = 0
alter VD6 dc = 0
alter VD7 dc = 3.3
op
echo DAC 152 $&v(out)
alter VD0 dc = 3.3
alter VD1 dc = 0
alter VD2 dc = 0
alter VD3 dc = 3.3
alter VD4 dc = 3.3
alter VD5 dc = 0
alter VD6 dc = 0
alter VD7 dc = 3.3
op
echo DAC 153 $&v(out)
alter VD0 dc = 0
alter VD1 dc = 3.3
alter VD2 dc = 0
alter VD3 dc = 3.3
alter VD4 dc = 3.3
alter VD5 dc = 0
alter VD6 dc = 0
alter VD7 dc = 3.3
op
echo DAC 154 $&v(out)
alter VD0 dc = 3.3
alter VD1 dc = 3.3
alter VD2 dc = 0
alter VD3 dc = 3.3
alter VD4 dc = 3.3
alter VD5 dc = 0
alter VD6 dc = 0
alter VD7 dc = 3.3
op
echo DAC 155 $&v(out)
alter VD0 dc = 0
alter VD1 dc = 0
alter VD2 dc = 3.3
alter VD3 dc = 3.3
alter VD4 dc = 3.3
alter VD5 dc = 0
alter VD6 dc = 0
alter VD7 dc = 3.3
op
echo DAC 156 $&v(out)
alter VD0 dc = 3.3
alter VD1 dc = 0
alter VD2 dc = 3.3
alter VD3 dc = 3.3
alter VD4 dc = 3.3
alter VD5 dc = 0
alter VD6 dc = 0
alter VD7 dc = 3.3
op
echo DAC 157 $&v(out)
alter VD0 dc = 0
alter VD1 dc = 3.3
alter VD2 dc = 3.3
alter VD3 dc = 3.3
alter VD4 dc = 3.3
alter VD5 dc = 0
alter VD6 dc = 0
alter VD7 dc = 3.3
op
echo DAC 158 $&v(out)
alter VD0 dc = 3.3
alter VD1 dc = 3.3
alter VD2 dc = 3.3
alter VD3 dc = 3.3
alter VD4 dc = 3.3
alter VD5 dc = 0
alter VD6 dc = 0
alter VD7 dc = 3.3
op
echo DAC 159 $&v(out)
alter VD0 dc = 0
alter VD1 dc = 0
alter VD2 dc = 0
alter VD3 dc = 0
alter VD4 dc = 0
alter VD5 dc = 3.3
alter VD6 dc = 0
alter VD7 dc = 3.3
op
echo DAC 160 $&v(out)
alter VD0 dc = 3.3
alter VD1 dc = 0
alter VD2 dc = 0
alter VD3 dc = 0
alter VD4 dc = 0
alter VD5 dc = 3.3
alter VD6 dc = 0
alter VD7 dc = 3.3
op
echo DAC 161 $&v(out)
alter VD0 dc = 0
alter VD1 dc = 3.3
alter VD2 dc = 0
alter VD3 dc = 0
alter VD4 dc = 0
alter VD5 dc = 3.3
alter VD6 dc = 0
alter VD7 dc = 3.3
op
echo DAC 162 $&v(out)
alter VD0 dc = 3.3
alter VD1 dc = 3.3
alter VD2 dc = 0
alter VD3 dc = 0
alter VD4 dc = 0
alter VD5 dc = 3.3
alter VD6 dc = 0
alter VD7 dc = 3.3
op
echo DAC 163 $&v(out)
alter VD0 dc = 0
alter VD1 dc = 0
alter VD2 dc = 3.3
alter VD3 dc = 0
alter VD4 dc = 0
alter VD5 dc = 3.3
alter VD6 dc = 0
alter VD7 dc = 3.3
op
echo DAC 164 $&v(out)
alter VD0 dc = 3.3
alter VD1 dc = 0
alter VD2 dc = 3.3
alter VD3 dc = 0
alter VD4 dc = 0
alter VD5 dc = 3.3
alter VD6 dc = 0
alter VD7 dc = 3.3
op
echo DAC 165 $&v(out)
alter VD0 dc = 0
alter VD1 dc = 3.3
alter VD2 dc = 3.3
alter VD3 dc = 0
alter VD4 dc = 0
alter VD5 dc = 3.3
alter VD6 dc = 0
alter VD7 dc = 3.3
op
echo DAC 166 $&v(out)
alter VD0 dc = 3.3
alter VD1 dc = 3.3
alter VD2 dc = 3.3
alter VD3 dc = 0
alter VD4 dc = 0
alter VD5 dc = 3.3
alter VD6 dc = 0
alter VD7 dc = 3.3
op
echo DAC 167 $&v(out)
alter VD0 dc = 0
alter VD1 dc = 0
alter VD2 dc = 0
alter VD3 dc = 3.3
alter VD4 dc = 0
alter VD5 dc = 3.3
alter VD6 dc = 0
alter VD7 dc = 3.3
op
echo DAC 168 $&v(out)
alter VD0 dc = 3.3
alter VD1 dc = 0
alter VD2 dc = 0
alter VD3 dc = 3.3
alter VD4 dc = 0
alter VD5 dc = 3.3
alter VD6 dc = 0
alter VD7 dc = 3.3
op
echo DAC 169 $&v(out)
alter VD0 dc = 0
alter VD1 dc = 3.3
alter VD2 dc = 0
alter VD3 dc = 3.3
alter VD4 dc = 0
alter VD5 dc = 3.3
alter VD6 dc = 0
alter VD7 dc = 3.3
op
echo DAC 170 $&v(out)
alter VD0 dc = 3.3
alter VD1 dc = 3.3
alter VD2 dc = 0
alter VD3 dc = 3.3
alter VD4 dc = 0
alter VD5 dc = 3.3
alter VD6 dc = 0
alter VD7 dc = 3.3
op
echo DAC 171 $&v(out)
alter VD0 dc = 0
alter VD1 dc = 0
alter VD2 dc = 3.3
alter VD3 dc = 3.3
alter VD4 dc = 0
alter VD5 dc = 3.3
alter VD6 dc = 0
alter VD7 dc = 3.3
op
echo DAC 172 $&v(out)
alter VD0 dc = 3.3
alter VD1 dc = 0
alter VD2 dc = 3.3
alter VD3 dc = 3.3
alter VD4 dc = 0
alter VD5 dc = 3.3
alter VD6 dc = 0
alter VD7 dc = 3.3
op
echo DAC 173 $&v(out)
alter VD0 dc = 0
alter VD1 dc = 3.3
alter VD2 dc = 3.3
alter VD3 dc = 3.3
alter VD4 dc = 0
alter VD5 dc = 3.3
alter VD6 dc = 0
alter VD7 dc = 3.3
op
echo DAC 174 $&v(out)
alter VD0 dc = 3.3
alter VD1 dc = 3.3
alter VD2 dc = 3.3
alter VD3 dc = 3.3
alter VD4 dc = 0
alter VD5 dc = 3.3
alter VD6 dc = 0
alter VD7 dc = 3.3
op
echo DAC 175 $&v(out)
alter VD0 dc = 0
alter VD1 dc = 0
alter VD2 dc = 0
alter VD3 dc = 0
alter VD4 dc = 3.3
alter VD5 dc = 3.3
alter VD6 dc = 0
alter VD7 dc = 3.3
op
echo DAC 176 $&v(out)
alter VD0 dc = 3.3
alter VD1 dc = 0
alter VD2 dc = 0
alter VD3 dc = 0
alter VD4 dc = 3.3
alter VD5 dc = 3.3
alter VD6 dc = 0
alter VD7 dc = 3.3
op
echo DAC 177 $&v(out)
alter VD0 dc = 0
alter VD1 dc = 3.3
alter VD2 dc = 0
alter VD3 dc = 0
alter VD4 dc = 3.3
alter VD5 dc = 3.3
alter VD6 dc = 0
alter VD7 dc = 3.3
op
echo DAC 178 $&v(out)
alter VD0 dc = 3.3
alter VD1 dc = 3.3
alter VD2 dc = 0
alter VD3 dc = 0
alter VD4 dc = 3.3
alter VD5 dc = 3.3
alter VD6 dc = 0
alter VD7 dc = 3.3
op
echo DAC 179 $&v(out)
alter VD0 dc = 0
alter VD1 dc = 0
alter VD2 dc = 3.3
alter VD3 dc = 0
alter VD4 dc = 3.3
alter VD5 dc = 3.3
alter VD6 dc = 0
alter VD7 dc = 3.3
op
echo DAC 180 $&v(out)
alter VD0 dc = 3.3
alter VD1 dc = 0
alter VD2 dc = 3.3
alter VD3 dc = 0
alter VD4 dc = 3.3
alter VD5 dc = 3.3
alter VD6 dc = 0
alter VD7 dc = 3.3
op
echo DAC 181 $&v(out)
alter VD0 dc = 0
alter VD1 dc = 3.3
alter VD2 dc = 3.3
alter VD3 dc = 0
alter VD4 dc = 3.3
alter VD5 dc = 3.3
alter VD6 dc = 0
alter VD7 dc = 3.3
op
echo DAC 182 $&v(out)
alter VD0 dc = 3.3
alter VD1 dc = 3.3
alter VD2 dc = 3.3
alter VD3 dc = 0
alter VD4 dc = 3.3
alter VD5 dc = 3.3
alter VD6 dc = 0
alter VD7 dc = 3.3
op
echo DAC 183 $&v(out)
alter VD0 dc = 0
alter VD1 dc = 0
alter VD2 dc = 0
alter VD3 dc = 3.3
alter VD4 dc = 3.3
alter VD5 dc = 3.3
alter VD6 dc = 0
alter VD7 dc = 3.3
op
echo DAC 184 $&v(out)
alter VD0 dc = 3.3
alter VD1 dc = 0
alter VD2 dc = 0
alter VD3 dc = 3.3
alter VD4 dc = 3.3
alter VD5 dc = 3.3
alter VD6 dc = 0
alter VD7 dc = 3.3
op
echo DAC 185 $&v(out)
alter VD0 dc = 0
alter VD1 dc = 3.3
alter VD2 dc = 0
alter VD3 dc = 3.3
alter VD4 dc = 3.3
alter VD5 dc = 3.3
alter VD6 dc = 0
alter VD7 dc = 3.3
op
echo DAC 186 $&v(out)
alter VD0 dc = 3.3
alter VD1 dc = 3.3
alter VD2 dc = 0
alter VD3 dc = 3.3
alter VD4 dc = 3.3
alter VD5 dc = 3.3
alter VD6 dc = 0
alter VD7 dc = 3.3
op
echo DAC 187 $&v(out)
alter VD0 dc = 0
alter VD1 dc = 0
alter VD2 dc = 3.3
alter VD3 dc = 3.3
alter VD4 dc = 3.3
alter VD5 dc = 3.3
alter VD6 dc = 0
alter VD7 dc = 3.3
op
echo DAC 188 $&v(out)
alter VD0 dc = 3.3
alter VD1 dc = 0
alter VD2 dc = 3.3
alter VD3 dc = 3.3
alter VD4 dc = 3.3
alter VD5 dc = 3.3
alter VD6 dc = 0
alter VD7 dc = 3.3
op
echo DAC 189 $&v(out)
alter VD0 dc = 0
alter VD1 dc = 3.3
alter VD2 dc = 3.3
alter VD3 dc = 3.3
alter VD4 dc = 3.3
alter VD5 dc = 3.3
alter VD6 dc = 0
alter VD7 dc = 3.3
op
echo DAC 190 $&v(out)
alter VD0 dc = 3.3
alter VD1 dc = 3.3
alter VD2 dc = 3.3
alter VD3 dc = 3.3
alter VD4 dc = 3.3
alter VD5 dc = 3.3
alter VD6 dc = 0
alter VD7 dc = 3.3
op
echo DAC 191 $&v(out)
alter VD0 dc = 0
alter VD1 dc = 0
alter VD2 dc = 0
alter VD3 dc = 0
alter VD4 dc = 0
alter VD5 dc = 0
alter VD6 dc = 3.3
alter VD7 dc = 3.3
op
echo DAC 192 $&v(out)
alter VD0 dc = 3.3
alter VD1 dc = 0
alter VD2 dc = 0
alter VD3 dc = 0
alter VD4 dc = 0
alter VD5 dc = 0
alter VD6 dc = 3.3
alter VD7 dc = 3.3
op
echo DAC 193 $&v(out)
alter VD0 dc = 0
alter VD1 dc = 3.3
alter VD2 dc = 0
alter VD3 dc = 0
alter VD4 dc = 0
alter VD5 dc = 0
alter VD6 dc = 3.3
alter VD7 dc = 3.3
op
echo DAC 194 $&v(out)
alter VD0 dc = 3.3
alter VD1 dc = 3.3
alter VD2 dc = 0
alter VD3 dc = 0
alter VD4 dc = 0
alter VD5 dc = 0
alter VD6 dc = 3.3
alter VD7 dc = 3.3
op
echo DAC 195 $&v(out)
alter VD0 dc = 0
alter VD1 dc = 0
alter VD2 dc = 3.3
alter VD3 dc = 0
alter VD4 dc = 0
alter VD5 dc = 0
alter VD6 dc = 3.3
alter VD7 dc = 3.3
op
echo DAC 196 $&v(out)
alter VD0 dc = 3.3
alter VD1 dc = 0
alter VD2 dc = 3.3
alter VD3 dc = 0
alter VD4 dc = 0
alter VD5 dc = 0
alter VD6 dc = 3.3
alter VD7 dc = 3.3
op
echo DAC 197 $&v(out)
alter VD0 dc = 0
alter VD1 dc = 3.3
alter VD2 dc = 3.3
alter VD3 dc = 0
alter VD4 dc = 0
alter VD5 dc = 0
alter VD6 dc = 3.3
alter VD7 dc = 3.3
op
echo DAC 198 $&v(out)
alter VD0 dc = 3.3
alter VD1 dc = 3.3
alter VD2 dc = 3.3
alter VD3 dc = 0
alter VD4 dc = 0
alter VD5 dc = 0
alter VD6 dc = 3.3
alter VD7 dc = 3.3
op
echo DAC 199 $&v(out)
alter VD0 dc = 0
alter VD1 dc = 0
alter VD2 dc = 0
alter VD3 dc = 3.3
alter VD4 dc = 0
alter VD5 dc = 0
alter VD6 dc = 3.3
alter VD7 dc = 3.3
op
echo DAC 200 $&v(out)
alter VD0 dc = 3.3
alter VD1 dc = 0
alter VD2 dc = 0
alter VD3 dc = 3.3
alter VD4 dc = 0
alter VD5 dc = 0
alter VD6 dc = 3.3
alter VD7 dc = 3.3
op
echo DAC 201 $&v(out)
alter VD0 dc = 0
alter VD1 dc = 3.3
alter VD2 dc = 0
alter VD3 dc = 3.3
alter VD4 dc = 0
alter VD5 dc = 0
alter VD6 dc = 3.3
alter VD7 dc = 3.3
op
echo DAC 202 $&v(out)
alter VD0 dc = 3.3
alter VD1 dc = 3.3
alter VD2 dc = 0
alter VD3 dc = 3.3
alter VD4 dc = 0
alter VD5 dc = 0
alter VD6 dc = 3.3
alter VD7 dc = 3.3
op
echo DAC 203 $&v(out)
alter VD0 dc = 0
alter VD1 dc = 0
alter VD2 dc = 3.3
alter VD3 dc = 3.3
alter VD4 dc = 0
alter VD5 dc = 0
alter VD6 dc = 3.3
alter VD7 dc = 3.3
op
echo DAC 204 $&v(out)
alter VD0 dc = 3.3
alter VD1 dc = 0
alter VD2 dc = 3.3
alter VD3 dc = 3.3
alter VD4 dc = 0
alter VD5 dc = 0
alter VD6 dc = 3.3
alter VD7 dc = 3.3
op
echo DAC 205 $&v(out)
alter VD0 dc = 0
alter VD1 dc = 3.3
alter VD2 dc = 3.3
alter VD3 dc = 3.3
alter VD4 dc = 0
alter VD5 dc = 0
alter VD6 dc = 3.3
alter VD7 dc = 3.3
op
echo DAC 206 $&v(out)
alter VD0 dc = 3.3
alter VD1 dc = 3.3
alter VD2 dc = 3.3
alter VD3 dc = 3.3
alter VD4 dc = 0
alter VD5 dc = 0
alter VD6 dc = 3.3
alter VD7 dc = 3.3
op
echo DAC 207 $&v(out)
alter VD0 dc = 0
alter VD1 dc = 0
alter VD2 dc = 0
alter VD3 dc = 0
alter VD4 dc = 3.3
alter VD5 dc = 0
alter VD6 dc = 3.3
alter VD7 dc = 3.3
op
echo DAC 208 $&v(out)
alter VD0 dc = 3.3
alter VD1 dc = 0
alter VD2 dc = 0
alter VD3 dc = 0
alter VD4 dc = 3.3
alter VD5 dc = 0
alter VD6 dc = 3.3
alter VD7 dc = 3.3
op
echo DAC 209 $&v(out)
alter VD0 dc = 0
alter VD1 dc = 3.3
alter VD2 dc = 0
alter VD3 dc = 0
alter VD4 dc = 3.3
alter VD5 dc = 0
alter VD6 dc = 3.3
alter VD7 dc = 3.3
op
echo DAC 210 $&v(out)
alter VD0 dc = 3.3
alter VD1 dc = 3.3
alter VD2 dc = 0
alter VD3 dc = 0
alter VD4 dc = 3.3
alter VD5 dc = 0
alter VD6 dc = 3.3
alter VD7 dc = 3.3
op
echo DAC 211 $&v(out)
alter VD0 dc = 0
alter VD1 dc = 0
alter VD2 dc = 3.3
alter VD3 dc = 0
alter VD4 dc = 3.3
alter VD5 dc = 0
alter VD6 dc = 3.3
alter VD7 dc = 3.3
op
echo DAC 212 $&v(out)
alter VD0 dc = 3.3
alter VD1 dc = 0
alter VD2 dc = 3.3
alter VD3 dc = 0
alter VD4 dc = 3.3
alter VD5 dc = 0
alter VD6 dc = 3.3
alter VD7 dc = 3.3
op
echo DAC 213 $&v(out)
alter VD0 dc = 0
alter VD1 dc = 3.3
alter VD2 dc = 3.3
alter VD3 dc = 0
alter VD4 dc = 3.3
alter VD5 dc = 0
alter VD6 dc = 3.3
alter VD7 dc = 3.3
op
echo DAC 214 $&v(out)
alter VD0 dc = 3.3
alter VD1 dc = 3.3
alter VD2 dc = 3.3
alter VD3 dc = 0
alter VD4 dc = 3.3
alter VD5 dc = 0
alter VD6 dc = 3.3
alter VD7 dc = 3.3
op
echo DAC 215 $&v(out)
alter VD0 dc = 0
alter VD1 dc = 0
alter VD2 dc = 0
alter VD3 dc = 3.3
alter VD4 dc = 3.3
alter VD5 dc = 0
alter VD6 dc = 3.3
alter VD7 dc = 3.3
op
echo DAC 216 $&v(out)
alter VD0 dc = 3.3
alter VD1 dc = 0
alter VD2 dc = 0
alter VD3 dc = 3.3
alter VD4 dc = 3.3
alter VD5 dc = 0
alter VD6 dc = 3.3
alter VD7 dc = 3.3
op
echo DAC 217 $&v(out)
alter VD0 dc = 0
alter VD1 dc = 3.3
alter VD2 dc = 0
alter VD3 dc = 3.3
alter VD4 dc = 3.3
alter VD5 dc = 0
alter VD6 dc = 3.3
alter VD7 dc = 3.3
op
echo DAC 218 $&v(out)
alter VD0 dc = 3.3
alter VD1 dc = 3.3
alter VD2 dc = 0
alter VD3 dc = 3.3
alter VD4 dc = 3.3
alter VD5 dc = 0
alter VD6 dc = 3.3
alter VD7 dc = 3.3
op
echo DAC 219 $&v(out)
alter VD0 dc = 0
alter VD1 dc = 0
alter VD2 dc = 3.3
alter VD3 dc = 3.3
alter VD4 dc = 3.3
alter VD5 dc = 0
alter VD6 dc = 3.3
alter VD7 dc = 3.3
op
echo DAC 220 $&v(out)
alter VD0 dc = 3.3
alter VD1 dc = 0
alter VD2 dc = 3.3
alter VD3 dc = 3.3
alter VD4 dc = 3.3
alter VD5 dc = 0
alter VD6 dc = 3.3
alter VD7 dc = 3.3
op
echo DAC 221 $&v(out)
alter VD0 dc = 0
alter VD1 dc = 3.3
alter VD2 dc = 3.3
alter VD3 dc = 3.3
alter VD4 dc = 3.3
alter VD5 dc = 0
alter VD6 dc = 3.3
alter VD7 dc = 3.3
op
echo DAC 222 $&v(out)
alter VD0 dc = 3.3
alter VD1 dc = 3.3
alter VD2 dc = 3.3
alter VD3 dc = 3.3
alter VD4 dc = 3.3
alter VD5 dc = 0
alter VD6 dc = 3.3
alter VD7 dc = 3.3
op
echo DAC 223 $&v(out)
alter VD0 dc = 0
alter VD1 dc = 0
alter VD2 dc = 0
alter VD3 dc = 0
alter VD4 dc = 0
alter VD5 dc = 3.3
alter VD6 dc = 3.3
alter VD7 dc = 3.3
op
echo DAC 224 $&v(out)
alter VD0 dc = 3.3
alter VD1 dc = 0
alter VD2 dc = 0
alter VD3 dc = 0
alter VD4 dc = 0
alter VD5 dc = 3.3
alter VD6 dc = 3.3
alter VD7 dc = 3.3
op
echo DAC 225 $&v(out)
alter VD0 dc = 0
alter VD1 dc = 3.3
alter VD2 dc = 0
alter VD3 dc = 0
alter VD4 dc = 0
alter VD5 dc = 3.3
alter VD6 dc = 3.3
alter VD7 dc = 3.3
op
echo DAC 226 $&v(out)
alter VD0 dc = 3.3
alter VD1 dc = 3.3
alter VD2 dc = 0
alter VD3 dc = 0
alter VD4 dc = 0
alter VD5 dc = 3.3
alter VD6 dc = 3.3
alter VD7 dc = 3.3
op
echo DAC 227 $&v(out)
alter VD0 dc = 0
alter VD1 dc = 0
alter VD2 dc = 3.3
alter VD3 dc = 0
alter VD4 dc = 0
alter VD5 dc = 3.3
alter VD6 dc = 3.3
alter VD7 dc = 3.3
op
echo DAC 228 $&v(out)
alter VD0 dc = 3.3
alter VD1 dc = 0
alter VD2 dc = 3.3
alter VD3 dc = 0
alter VD4 dc = 0
alter VD5 dc = 3.3
alter VD6 dc = 3.3
alter VD7 dc = 3.3
op
echo DAC 229 $&v(out)
alter VD0 dc = 0
alter VD1 dc = 3.3
alter VD2 dc = 3.3
alter VD3 dc = 0
alter VD4 dc = 0
alter VD5 dc = 3.3
alter VD6 dc = 3.3
alter VD7 dc = 3.3
op
echo DAC 230 $&v(out)
alter VD0 dc = 3.3
alter VD1 dc = 3.3
alter VD2 dc = 3.3
alter VD3 dc = 0
alter VD4 dc = 0
alter VD5 dc = 3.3
alter VD6 dc = 3.3
alter VD7 dc = 3.3
op
echo DAC 231 $&v(out)
alter VD0 dc = 0
alter VD1 dc = 0
alter VD2 dc = 0
alter VD3 dc = 3.3
alter VD4 dc = 0
alter VD5 dc = 3.3
alter VD6 dc = 3.3
alter VD7 dc = 3.3
op
echo DAC 232 $&v(out)
alter VD0 dc = 3.3
alter VD1 dc = 0
alter VD2 dc = 0
alter VD3 dc = 3.3
alter VD4 dc = 0
alter VD5 dc = 3.3
alter VD6 dc = 3.3
alter VD7 dc = 3.3
op
echo DAC 233 $&v(out)
alter VD0 dc = 0
alter VD1 dc = 3.3
alter VD2 dc = 0
alter VD3 dc = 3.3
alter VD4 dc = 0
alter VD5 dc = 3.3
alter VD6 dc = 3.3
alter VD7 dc = 3.3
op
echo DAC 234 $&v(out)
alter VD0 dc = 3.3
alter VD1 dc = 3.3
alter VD2 dc = 0
alter VD3 dc = 3.3
alter VD4 dc = 0
alter VD5 dc = 3.3
alter VD6 dc = 3.3
alter VD7 dc = 3.3
op
echo DAC 235 $&v(out)
alter VD0 dc = 0
alter VD1 dc = 0
alter VD2 dc = 3.3
alter VD3 dc = 3.3
alter VD4 dc = 0
alter VD5 dc = 3.3
alter VD6 dc = 3.3
alter VD7 dc = 3.3
op
echo DAC 236 $&v(out)
alter VD0 dc = 3.3
alter VD1 dc = 0
alter VD2 dc = 3.3
alter VD3 dc = 3.3
alter VD4 dc = 0
alter VD5 dc = 3.3
alter VD6 dc = 3.3
alter VD7 dc = 3.3
op
echo DAC 237 $&v(out)
alter VD0 dc = 0
alter VD1 dc = 3.3
alter VD2 dc = 3.3
alter VD3 dc = 3.3
alter VD4 dc = 0
alter VD5 dc = 3.3
alter VD6 dc = 3.3
alter VD7 dc = 3.3
op
echo DAC 238 $&v(out)
alter VD0 dc = 3.3
alter VD1 dc = 3.3
alter VD2 dc = 3.3
alter VD3 dc = 3.3
alter VD4 dc = 0
alter VD5 dc = 3.3
alter VD6 dc = 3.3
alter VD7 dc = 3.3
op
echo DAC 239 $&v(out)
alter VD0 dc = 0
alter VD1 dc = 0
alter VD2 dc = 0
alter VD3 dc = 0
alter VD4 dc = 3.3
alter VD5 dc = 3.3
alter VD6 dc = 3.3
alter VD7 dc = 3.3
op
echo DAC 240 $&v(out)
alter VD0 dc = 3.3
alter VD1 dc = 0
alter VD2 dc = 0
alter VD3 dc = 0
alter VD4 dc = 3.3
alter VD5 dc = 3.3
alter VD6 dc = 3.3
alter VD7 dc = 3.3
op
echo DAC 241 $&v(out)
alter VD0 dc = 0
alter VD1 dc = 3.3
alter VD2 dc = 0
alter VD3 dc = 0
alter VD4 dc = 3.3
alter VD5 dc = 3.3
alter VD6 dc = 3.3
alter VD7 dc = 3.3
op
echo DAC 242 $&v(out)
alter VD0 dc = 3.3
alter VD1 dc = 3.3
alter VD2 dc = 0
alter VD3 dc = 0
alter VD4 dc = 3.3
alter VD5 dc = 3.3
alter VD6 dc = 3.3
alter VD7 dc = 3.3
op
echo DAC 243 $&v(out)
alter VD0 dc = 0
alter VD1 dc = 0
alter VD2 dc = 3.3
alter VD3 dc = 0
alter VD4 dc = 3.3
alter VD5 dc = 3.3
alter VD6 dc = 3.3
alter VD7 dc = 3.3
op
echo DAC 244 $&v(out)
alter VD0 dc = 3.3
alter VD1 dc = 0
alter VD2 dc = 3.3
alter VD3 dc = 0
alter VD4 dc = 3.3
alter VD5 dc = 3.3
alter VD6 dc = 3.3
alter VD7 dc = 3.3
op
echo DAC 245 $&v(out)
alter VD0 dc = 0
alter VD1 dc = 3.3
alter VD2 dc = 3.3
alter VD3 dc = 0
alter VD4 dc = 3.3
alter VD5 dc = 3.3
alter VD6 dc = 3.3
alter VD7 dc = 3.3
op
echo DAC 246 $&v(out)
alter VD0 dc = 3.3
alter VD1 dc = 3.3
alter VD2 dc = 3.3
alter VD3 dc = 0
alter VD4 dc = 3.3
alter VD5 dc = 3.3
alter VD6 dc = 3.3
alter VD7 dc = 3.3
op
echo DAC 247 $&v(out)
alter VD0 dc = 0
alter VD1 dc = 0
alter VD2 dc = 0
alter VD3 dc = 3.3
alter VD4 dc = 3.3
alter VD5 dc = 3.3
alter VD6 dc = 3.3
alter VD7 dc = 3.3
op
echo DAC 248 $&v(out)
alter VD0 dc = 3.3
alter VD1 dc = 0
alter VD2 dc = 0
alter VD3 dc = 3.3
alter VD4 dc = 3.3
alter VD5 dc = 3.3
alter VD6 dc = 3.3
alter VD7 dc = 3.3
op
echo DAC 249 $&v(out)
alter VD0 dc = 0
alter VD1 dc = 3.3
alter VD2 dc = 0
alter VD3 dc = 3.3
alter VD4 dc = 3.3
alter VD5 dc = 3.3
alter VD6 dc = 3.3
alter VD7 dc = 3.3
op
echo DAC 250 $&v(out)
alter VD0 dc = 3.3
alter VD1 dc = 3.3
alter VD2 dc = 0
alter VD3 dc = 3.3
alter VD4 dc = 3.3
alter VD5 dc = 3.3
alter VD6 dc = 3.3
alter VD7 dc = 3.3
op
echo DAC 251 $&v(out)
alter VD0 dc = 0
alter VD1 dc = 0
alter VD2 dc = 3.3
alter VD3 dc = 3.3
alter VD4 dc = 3.3
alter VD5 dc = 3.3
alter VD6 dc = 3.3
alter VD7 dc = 3.3
op
echo DAC 252 $&v(out)
alter VD0 dc = 3.3
alter VD1 dc = 0
alter VD2 dc = 3.3
alter VD3 dc = 3.3
alter VD4 dc = 3.3
alter VD5 dc = 3.3
alter VD6 dc = 3.3
alter VD7 dc = 3.3
op
echo DAC 253 $&v(out)
alter VD0 dc = 0
alter VD1 dc = 3.3
alter VD2 dc = 3.3
alter VD3 dc = 3.3
alter VD4 dc = 3.3
alter VD5 dc = 3.3
alter VD6 dc = 3.3
alter VD7 dc = 3.3
op
echo DAC 254 $&v(out)
alter VD0 dc = 3.3
alter VD1 dc = 3.3
alter VD2 dc = 3.3
alter VD3 dc = 3.3
alter VD4 dc = 3.3
alter VD5 dc = 3.3
alter VD6 dc = 3.3
alter VD7 dc = 3.3
op
echo DAC 255 $&v(out)
.endc

**** end user architecture code
**.ends
.end
